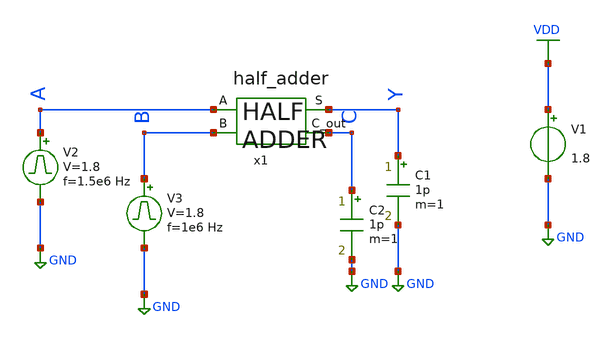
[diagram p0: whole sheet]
** sch_path: library/xschem/half_adder_tb.sch
**.subckt half_adder_tb
V1 VDD GND 1.8
V2 A GND pulse 0 1.8 '0.495/ 1.5e6 ' '0.01/1.5e6 ' '0.01/1.5e6 ' '0.49/1.5e6 ' '1/1.5e6 '
C1 Y GND 1p m=1
V3 B GND pulse 0 1.8 '0.495/ 1e6 ' '0.01/1e6 ' '0.01/1e6 ' '0.49/1e6 ' '1/1e6 '
C2 C GND 1p m=1
x1 A Y B C half_adder
**** begin user architecture code


.control
save all
tran 1n 2.2u
plot V(A)+2 V(B)+4 V(C)+6 V(Y)
.endc


** opencircuitdesign pdks install
.lib $::SKYWATER_MODELS/sky130.lib.spice tt


**** end user architecture code
**.ends

* expanding   symbol:  half_adder.sym # of pins=4
** sym_path: library/xschem/half_adder.sym
** sch_path: library/xschem/half_adder.sch
.subckt half_adder A S B C_out
*.opin S
*.ipin A
*.ipin B
*.opin C_out
x2 A B net1 net2 S xor2
x3 A net1 inv
x4 B net2 inv
x1 A net3 B nand2
x8 net3 C_out inv
.ends


* expanding   symbol:  xor2.sym # of pins=5
** sym_path: library/xschem/xor2.sym
** sch_path: library/xschem/xor2.sch
.subckt xor2 A B NOT_A NOT_B Y
*.opin Y
*.ipin A
*.ipin B
*.ipin NOT_A
*.ipin NOT_B
XM1 Y NOT_B net2 GND sky130_fd_pr__nfet_01v8 L=0.15 W=1 nf=1 ad='int((nf+1)/2) * W/nf * 0.29' as='int((nf+2)/2) * W/nf * 0.29'
+ pd='2*int((nf+1)/2) * (W/nf + 0.29)' ps='2*int((nf+2)/2) * (W/nf + 0.29)' nrd='0.29 / W' nrs='0.29 / W'
+ sa=0 sb=0 sd=0 mult=1 m=1
XM2 net1 A VDD VDD sky130_fd_pr__pfet_01v8 L=0.15 W=1 nf=1 ad='int((nf+1)/2) * W/nf * 0.29' as='int((nf+2)/2) * W/nf * 0.29'
+ pd='2*int((nf+1)/2) * (W/nf + 0.29)' ps='2*int((nf+2)/2) * (W/nf + 0.29)' nrd='0.29 / W' nrs='0.29 / W'
+ sa=0 sb=0 sd=0 mult=1 m=1
XM4 net2 NOT_A GND GND sky130_fd_pr__nfet_01v8 L=0.15 W=1 nf=1 ad='int((nf+1)/2) * W/nf * 0.29' as='int((nf+2)/2) * W/nf * 0.29'
+ pd='2*int((nf+1)/2) * (W/nf + 0.29)' ps='2*int((nf+2)/2) * (W/nf + 0.29)' nrd='0.29 / W' nrs='0.29 / W'
+ sa=0 sb=0 sd=0 mult=1 m=1
XM3 net1 B VDD VDD sky130_fd_pr__pfet_01v8 L=0.15 W=1 nf=1 ad='int((nf+1)/2) * W/nf * 0.29' as='int((nf+2)/2) * W/nf * 0.29'
+ pd='2*int((nf+1)/2) * (W/nf + 0.29)' ps='2*int((nf+2)/2) * (W/nf + 0.29)' nrd='0.29 / W' nrs='0.29 / W'
+ sa=0 sb=0 sd=0 mult=1 m=1
XM5 Y NOT_B net1 VDD sky130_fd_pr__pfet_01v8 L=0.15 W=1 nf=1 ad='int((nf+1)/2) * W/nf * 0.29' as='int((nf+2)/2) * W/nf * 0.29'
+ pd='2*int((nf+1)/2) * (W/nf + 0.29)' ps='2*int((nf+2)/2) * (W/nf + 0.29)' nrd='0.29 / W' nrs='0.29 / W'
+ sa=0 sb=0 sd=0 mult=1 m=1
XM6 Y NOT_A net1 VDD sky130_fd_pr__pfet_01v8 L=0.15 W=1 nf=1 ad='int((nf+1)/2) * W/nf * 0.29' as='int((nf+2)/2) * W/nf * 0.29'
+ pd='2*int((nf+1)/2) * (W/nf + 0.29)' ps='2*int((nf+2)/2) * (W/nf + 0.29)' nrd='0.29 / W' nrs='0.29 / W'
+ sa=0 sb=0 sd=0 mult=1 m=1
XM7 Y A net3 GND sky130_fd_pr__nfet_01v8 L=0.15 W=1 nf=1 ad='int((nf+1)/2) * W/nf * 0.29' as='int((nf+2)/2) * W/nf * 0.29'
+ pd='2*int((nf+1)/2) * (W/nf + 0.29)' ps='2*int((nf+2)/2) * (W/nf + 0.29)' nrd='0.29 / W' nrs='0.29 / W'
+ sa=0 sb=0 sd=0 mult=1 m=1
XM8 net3 B GND GND sky130_fd_pr__nfet_01v8 L=0.15 W=1 nf=1 ad='int((nf+1)/2) * W/nf * 0.29' as='int((nf+2)/2) * W/nf * 0.29'
+ pd='2*int((nf+1)/2) * (W/nf + 0.29)' ps='2*int((nf+2)/2) * (W/nf + 0.29)' nrd='0.29 / W' nrs='0.29 / W'
+ sa=0 sb=0 sd=0 mult=1 m=1
.ends


* expanding   symbol:  inv.sym # of pins=2
** sym_path: library/xschem/inv.sym
** sch_path: library/xschem/inv.sch
.subckt inv A Y
*.opin Y
*.ipin A
XM1 Y A GND GND sky130_fd_pr__nfet_01v8 L=0.15 W=1 nf=1 ad='int((nf+1)/2) * W/nf * 0.29' as='int((nf+2)/2) * W/nf * 0.29'
+ pd='2*int((nf+1)/2) * (W/nf + 0.29)' ps='2*int((nf+2)/2) * (W/nf + 0.29)' nrd='0.29 / W' nrs='0.29 / W'
+ sa=0 sb=0 sd=0 mult=1 m=1
XM2 Y A VDD VDD sky130_fd_pr__pfet_01v8 L=0.15 W=1 nf=1 ad='int((nf+1)/2) * W/nf * 0.29' as='int((nf+2)/2) * W/nf * 0.29'
+ pd='2*int((nf+1)/2) * (W/nf + 0.29)' ps='2*int((nf+2)/2) * (W/nf + 0.29)' nrd='0.29 / W' nrs='0.29 / W'
+ sa=0 sb=0 sd=0 mult=1 m=1
.ends


* expanding   symbol:  nand2.sym # of pins=3
** sym_path: library/xschem/nand2.sym
** sch_path: library/xschem/nand2.sch
.subckt nand2 A Y B
*.opin Y
*.ipin A
*.ipin B
XM1 Y B net1 GND sky130_fd_pr__nfet_01v8 L=0.15 W=1 nf=1 ad='int((nf+1)/2) * W/nf * 0.29' as='int((nf+2)/2) * W/nf * 0.29'
+ pd='2*int((nf+1)/2) * (W/nf + 0.29)' ps='2*int((nf+2)/2) * (W/nf + 0.29)' nrd='0.29 / W' nrs='0.29 / W'
+ sa=0 sb=0 sd=0 mult=1 m=1
XM2 Y B VDD VDD sky130_fd_pr__pfet_01v8 L=0.15 W=1 nf=1 ad='int((nf+1)/2) * W/nf * 0.29' as='int((nf+2)/2) * W/nf * 0.29'
+ pd='2*int((nf+1)/2) * (W/nf + 0.29)' ps='2*int((nf+2)/2) * (W/nf + 0.29)' nrd='0.29 / W' nrs='0.29 / W'
+ sa=0 sb=0 sd=0 mult=1 m=1
XM3 Y A VDD VDD sky130_fd_pr__pfet_01v8 L=0.15 W=1 nf=1 ad='int((nf+1)/2) * W/nf * 0.29' as='int((nf+2)/2) * W/nf * 0.29'
+ pd='2*int((nf+1)/2) * (W/nf + 0.29)' ps='2*int((nf+2)/2) * (W/nf + 0.29)' nrd='0.29 / W' nrs='0.29 / W'
+ sa=0 sb=0 sd=0 mult=1 m=1
XM4 net1 A GND GND sky130_fd_pr__nfet_01v8 L=0.15 W=1 nf=1 ad='int((nf+1)/2) * W/nf * 0.29' as='int((nf+2)/2) * W/nf * 0.29'
+ pd='2*int((nf+1)/2) * (W/nf + 0.29)' ps='2*int((nf+2)/2) * (W/nf + 0.29)' nrd='0.29 / W' nrs='0.29 / W'
+ sa=0 sb=0 sd=0 mult=1 m=1
.ends

.GLOBAL VDD
.GLOBAL GND
.end
